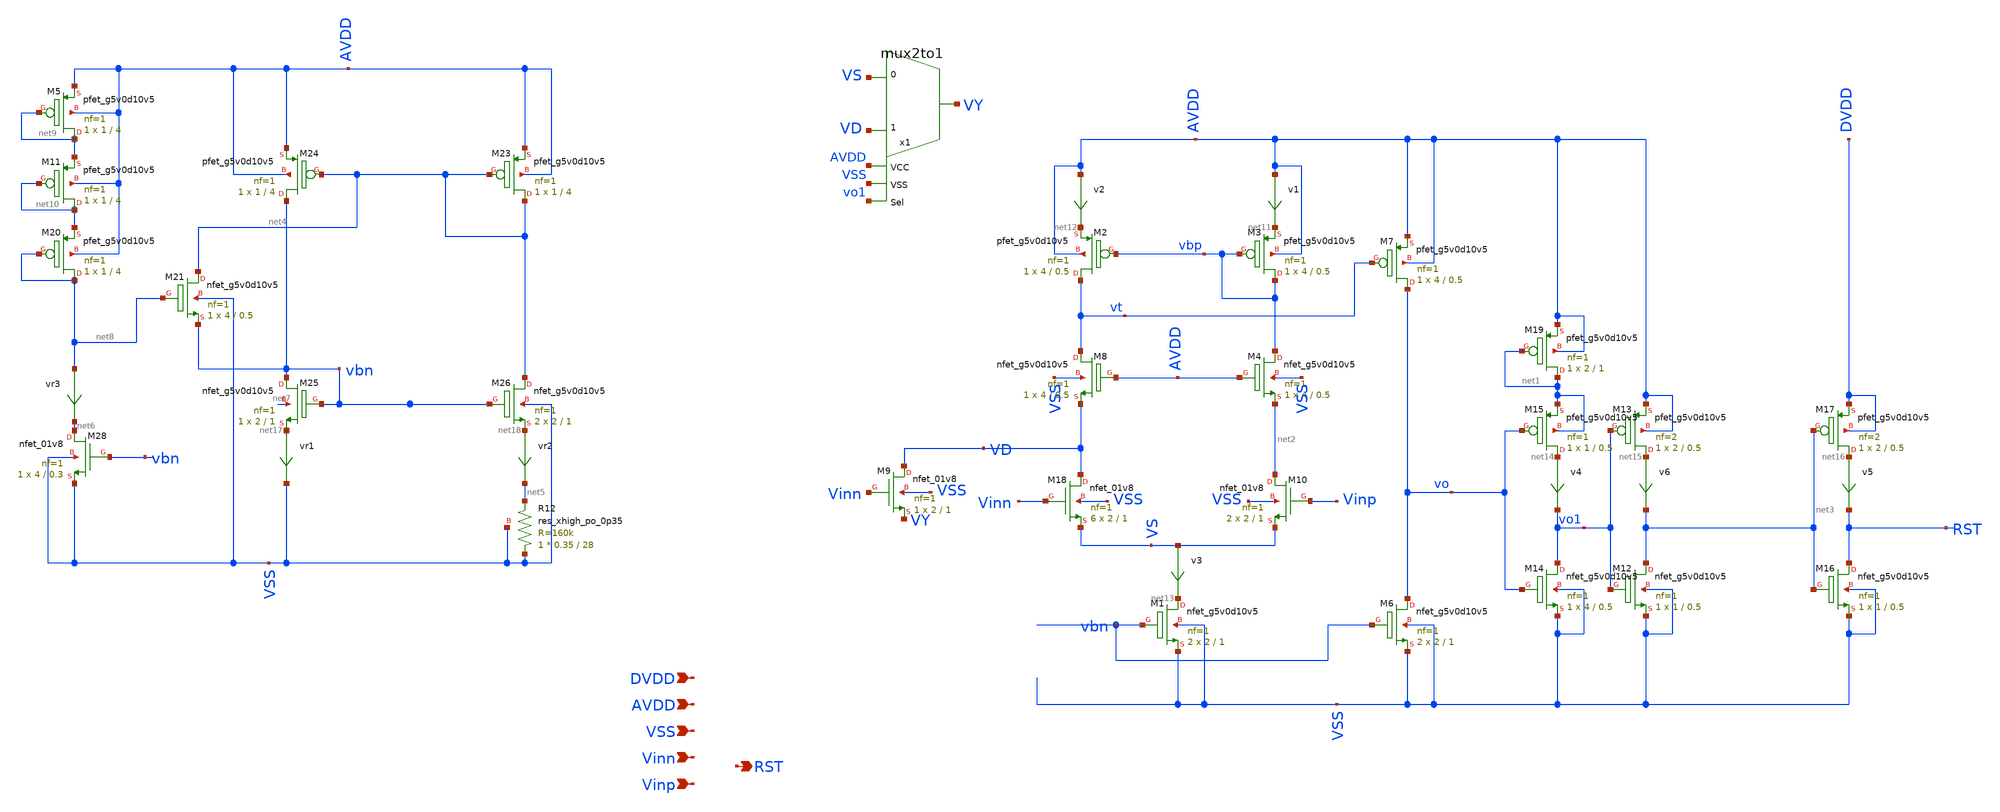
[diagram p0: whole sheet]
** sch_path: xschem/comparator_final.sch
**.subckt comparator_final AVDD RST VSS Vinn Vinp DVDD
*.ipin AVDD
*.opin RST
*.ipin VSS
*.ipin Vinn
*.ipin Vinp
*.ipin DVDD
v1 AVDD net11 0
.save i(v1)
v2 AVDD net12 0
.save i(v2)
XM1 net13 vbn VSS VSS sky130_fd_pr__nfet_g5v0d10v5 L=1 W=2 nf=1 ad='int((nf+1)/2) * W/nf * 0.29' as='int((nf+2)/2) * W/nf * 0.29'
+ pd='2*int((nf+1)/2) * (W/nf + 0.29)' ps='2*int((nf+2)/2) * (W/nf + 0.29)' nrd='0.29 / W' nrs='0.29 / W'
+ sa=0 sb=0 sd=0 mult=2 m=2
XM3 vbp vbp net11 AVDD sky130_fd_pr__pfet_g5v0d10v5 L=0.5 W=4 nf=1 ad='int((nf+1)/2) * W/nf * 0.29' as='int((nf+2)/2) * W/nf * 0.29'
+ pd='2*int((nf+1)/2) * (W/nf + 0.29)' ps='2*int((nf+2)/2) * (W/nf + 0.29)' nrd='0.29 / W' nrs='0.29 / W'
+ sa=0 sb=0 sd=0 mult=1 m=1
XM2 vt vbp net12 AVDD sky130_fd_pr__pfet_g5v0d10v5 L=0.5 W=4 nf=1 ad='int((nf+1)/2) * W/nf * 0.29' as='int((nf+2)/2) * W/nf * 0.29'
+ pd='2*int((nf+1)/2) * (W/nf + 0.29)' ps='2*int((nf+2)/2) * (W/nf + 0.29)' nrd='0.29 / W' nrs='0.29 / W'
+ sa=0 sb=0 sd=0 mult=1 m=1
v4 net14 vo1 0
.save i(v4)
XM7 vo vt AVDD AVDD sky130_fd_pr__pfet_g5v0d10v5 L=0.5 W=4 nf=1 ad='int((nf+1)/2) * W/nf * 0.29' as='int((nf+2)/2) * W/nf * 0.29'
+ pd='2*int((nf+1)/2) * (W/nf + 0.29)' ps='2*int((nf+2)/2) * (W/nf + 0.29)' nrd='0.29 / W' nrs='0.29 / W'
+ sa=0 sb=0 sd=0 mult=1 m=1
v3 VS net13 0
.save i(v3)
x1 VD VS VY AVDD VSS vo1 mux2to1
XM6 vo vbn VSS VSS sky130_fd_pr__nfet_g5v0d10v5 L=1 W=2 nf=1 ad='int((nf+1)/2) * W/nf * 0.29' as='int((nf+2)/2) * W/nf * 0.29'
+ pd='2*int((nf+1)/2) * (W/nf + 0.29)' ps='2*int((nf+2)/2) * (W/nf + 0.29)' nrd='0.29 / W' nrs='0.29 / W'
+ sa=0 sb=0 sd=0 mult=2 m=2
v6 net15 net3 0
.save i(v6)
XM14 vo1 vo VSS VSS sky130_fd_pr__nfet_g5v0d10v5 L=0.5 W=4 nf=1 ad='int((nf+1)/2) * W/nf * 0.29' as='int((nf+2)/2) * W/nf * 0.29'
+ pd='2*int((nf+1)/2) * (W/nf + 0.29)' ps='2*int((nf+2)/2) * (W/nf + 0.29)' nrd='0.29 / W' nrs='0.29 / W'
+ sa=0 sb=0 sd=0 mult=1 m=1
XM15 net14 vo net1 net1 sky130_fd_pr__pfet_g5v0d10v5 L=0.5 W=1 nf=1 ad='int((nf+1)/2) * W/nf * 0.29'
+ as='int((nf+2)/2) * W/nf * 0.29' pd='2*int((nf+1)/2) * (W/nf + 0.29)' ps='2*int((nf+2)/2) * (W/nf + 0.29)'
+ nrd='0.29 / W' nrs='0.29 / W' sa=0 sb=0 sd=0 mult=1 m=1
XM12 net3 vo1 VSS VSS sky130_fd_pr__nfet_g5v0d10v5 L=0.5 W=1 nf=1 ad='int((nf+1)/2) * W/nf * 0.29' as='int((nf+2)/2) * W/nf * 0.29'
+ pd='2*int((nf+1)/2) * (W/nf + 0.29)' ps='2*int((nf+2)/2) * (W/nf + 0.29)' nrd='0.29 / W' nrs='0.29 / W'
+ sa=0 sb=0 sd=0 mult=1 m=1
XM13 net15 vo1 AVDD AVDD sky130_fd_pr__pfet_g5v0d10v5 L=0.5 W=2 nf=2 ad='int((nf+1)/2) * W/nf * 0.29'
+ as='int((nf+2)/2) * W/nf * 0.29' pd='2*int((nf+1)/2) * (W/nf + 0.29)' ps='2*int((nf+2)/2) * (W/nf + 0.29)'
+ nrd='0.29 / W' nrs='0.29 / W' sa=0 sb=0 sd=0 mult=1 m=1
v5 net16 RST 0
.save i(v5)
XM16 RST net3 VSS VSS sky130_fd_pr__nfet_g5v0d10v5 L=0.5 W=1 nf=1 ad='int((nf+1)/2) * W/nf * 0.29' as='int((nf+2)/2) * W/nf * 0.29'
+ pd='2*int((nf+1)/2) * (W/nf + 0.29)' ps='2*int((nf+2)/2) * (W/nf + 0.29)' nrd='0.29 / W' nrs='0.29 / W'
+ sa=0 sb=0 sd=0 mult=1 m=1
XM17 net16 net3 DVDD DVDD sky130_fd_pr__pfet_g5v0d10v5 L=0.5 W=2 nf=2 ad='int((nf+1)/2) * W/nf * 0.29'
+ as='int((nf+2)/2) * W/nf * 0.29' pd='2*int((nf+1)/2) * (W/nf + 0.29)' ps='2*int((nf+2)/2) * (W/nf + 0.29)'
+ nrd='0.29 / W' nrs='0.29 / W' sa=0 sb=0 sd=0 mult=1 m=1
XM4 vbp AVDD net2 VSS sky130_fd_pr__nfet_g5v0d10v5 L=0.5 W=4 nf=1 ad='int((nf+1)/2) * W/nf * 0.29' as='int((nf+2)/2) * W/nf * 0.29'
+ pd='2*int((nf+1)/2) * (W/nf + 0.29)' ps='2*int((nf+2)/2) * (W/nf + 0.29)' nrd='0.29 / W' nrs='0.29 / W'
+ sa=0 sb=0 sd=0 mult=1 m=1
XM8 vt AVDD VD VSS sky130_fd_pr__nfet_g5v0d10v5 L=0.5 W=4 nf=1 ad='int((nf+1)/2) * W/nf * 0.29' as='int((nf+2)/2) * W/nf * 0.29'
+ pd='2*int((nf+1)/2) * (W/nf + 0.29)' ps='2*int((nf+2)/2) * (W/nf + 0.29)' nrd='0.29 / W' nrs='0.29 / W'
+ sa=0 sb=0 sd=0 mult=1 m=1
XM19 net1 net1 AVDD AVDD sky130_fd_pr__pfet_g5v0d10v5 L=1 W=2 nf=1 ad='int((nf+1)/2) * W/nf * 0.29' as='int((nf+2)/2) * W/nf * 0.29'
+ pd='2*int((nf+1)/2) * (W/nf + 0.29)' ps='2*int((nf+2)/2) * (W/nf + 0.29)' nrd='0.29 / W' nrs='0.29 / W'
+ sa=0 sb=0 sd=0 mult=1 m=1
XM23 net4 net4 AVDD AVDD sky130_fd_pr__pfet_g5v0d10v5 L=4 W=1 nf=1 ad='int((nf+1)/2) * W/nf * 0.29' as='int((nf+2)/2) * W/nf * 0.29'
+ pd='2*int((nf+1)/2) * (W/nf + 0.29)' ps='2*int((nf+2)/2) * (W/nf + 0.29)' nrd='0.29 / W' nrs='0.29 / W'
+ sa=0 sb=0 sd=0 mult=1 m=1
XM24 vbn net4 AVDD AVDD sky130_fd_pr__pfet_g5v0d10v5 L=4 W=1 nf=1 ad='int((nf+1)/2) * W/nf * 0.29' as='int((nf+2)/2) * W/nf * 0.29'
+ pd='2*int((nf+1)/2) * (W/nf + 0.29)' ps='2*int((nf+2)/2) * (W/nf + 0.29)' nrd='0.29 / W' nrs='0.29 / W'
+ sa=0 sb=0 sd=0 mult=1 m=1
XR12 VSS net5 VSS sky130_fd_pr__res_xhigh_po_0p35 L=28 mult=1 m=1
vr1 net17 VSS 0
.save i(vr1)
vr2 net18 net5 0
.save i(vr2)
vr3 net8 net6 0
.save i(vr3)
XM25 vbn vbn net17 net7 sky130_fd_pr__nfet_g5v0d10v5 L=1 W=2 nf=1 ad='int((nf+1)/2) * W/nf * 0.29' as='int((nf+2)/2) * W/nf * 0.29'
+ pd='2*int((nf+1)/2) * (W/nf + 0.29)' ps='2*int((nf+2)/2) * (W/nf + 0.29)' nrd='0.29 / W' nrs='0.29 / W'
+ sa=0 sb=0 sd=0 mult=1 m=1
XM26 net4 vbn net18 VSS sky130_fd_pr__nfet_g5v0d10v5 L=1 W=2 nf=1 ad='int((nf+1)/2) * W/nf * 0.29' as='int((nf+2)/2) * W/nf * 0.29'
+ pd='2*int((nf+1)/2) * (W/nf + 0.29)' ps='2*int((nf+2)/2) * (W/nf + 0.29)' nrd='0.29 / W' nrs='0.29 / W'
+ sa=0 sb=0 sd=0 mult=2 m=2
XM28 net6 vbn VSS VSS sky130_fd_pr__nfet_01v8 L=0.3 W=4 nf=1 ad='int((nf+1)/2) * W/nf * 0.29' as='int((nf+2)/2) * W/nf * 0.29'
+ pd='2*int((nf+1)/2) * (W/nf + 0.29)' ps='2*int((nf+2)/2) * (W/nf + 0.29)' nrd='0.29 / W' nrs='0.29 / W'
+ sa=0 sb=0 sd=0 mult=1 m=1
XM18 VD Vinn VS VSS sky130_fd_pr__nfet_01v8 L=1 W=2 nf=1 ad='int((nf+1)/2) * W/nf * 0.29' as='int((nf+2)/2) * W/nf * 0.29'
+ pd='2*int((nf+1)/2) * (W/nf + 0.29)' ps='2*int((nf+2)/2) * (W/nf + 0.29)' nrd='0.29 / W' nrs='0.29 / W'
+ sa=0 sb=0 sd=0 mult=6 m=6
XM9 VD Vinn VY VSS sky130_fd_pr__nfet_01v8 L=1 W=2 nf=1 ad='int((nf+1)/2) * W/nf * 0.29' as='int((nf+2)/2) * W/nf * 0.29'
+ pd='2*int((nf+1)/2) * (W/nf + 0.29)' ps='2*int((nf+2)/2) * (W/nf + 0.29)' nrd='0.29 / W' nrs='0.29 / W'
+ sa=0 sb=0 sd=0 mult=1 m=1
XM10 net2 Vinp VS VSS sky130_fd_pr__nfet_01v8 L=1 W=2 nf=1 ad='int((nf+1)/2) * W/nf * 0.29' as='int((nf+2)/2) * W/nf * 0.29'
+ pd='2*int((nf+1)/2) * (W/nf + 0.29)' ps='2*int((nf+2)/2) * (W/nf + 0.29)' nrd='0.29 / W' nrs='0.29 / W'
+ sa=0 sb=0 sd=0 mult=2 m=2
XM5 net9 net9 AVDD AVDD sky130_fd_pr__pfet_g5v0d10v5 L=4 W=1 nf=1 ad='int((nf+1)/2) * W/nf * 0.29' as='int((nf+2)/2) * W/nf * 0.29'
+ pd='2*int((nf+1)/2) * (W/nf + 0.29)' ps='2*int((nf+2)/2) * (W/nf + 0.29)' nrd='0.29 / W' nrs='0.29 / W'
+ sa=0 sb=0 sd=0 mult=1 m=1
XM11 net10 net10 net9 AVDD sky130_fd_pr__pfet_g5v0d10v5 L=4 W=1 nf=1 ad='int((nf+1)/2) * W/nf * 0.29'
+ as='int((nf+2)/2) * W/nf * 0.29' pd='2*int((nf+1)/2) * (W/nf + 0.29)' ps='2*int((nf+2)/2) * (W/nf + 0.29)'
+ nrd='0.29 / W' nrs='0.29 / W' sa=0 sb=0 sd=0 mult=1 m=1
XM20 net8 net8 net10 AVDD sky130_fd_pr__pfet_g5v0d10v5 L=4 W=1 nf=1 ad='int((nf+1)/2) * W/nf * 0.29'
+ as='int((nf+2)/2) * W/nf * 0.29' pd='2*int((nf+1)/2) * (W/nf + 0.29)' ps='2*int((nf+2)/2) * (W/nf + 0.29)'
+ nrd='0.29 / W' nrs='0.29 / W' sa=0 sb=0 sd=0 mult=1 m=1
XM21 net4 net8 vbn VSS sky130_fd_pr__nfet_g5v0d10v5 L=0.5 W=4 nf=1 ad='int((nf+1)/2) * W/nf * 0.29' as='int((nf+2)/2) * W/nf * 0.29'
+ pd='2*int((nf+1)/2) * (W/nf + 0.29)' ps='2*int((nf+2)/2) * (W/nf + 0.29)' nrd='0.29 / W' nrs='0.29 / W'
+ sa=0 sb=0 sd=0 mult=1 m=1
**.ends
.end
